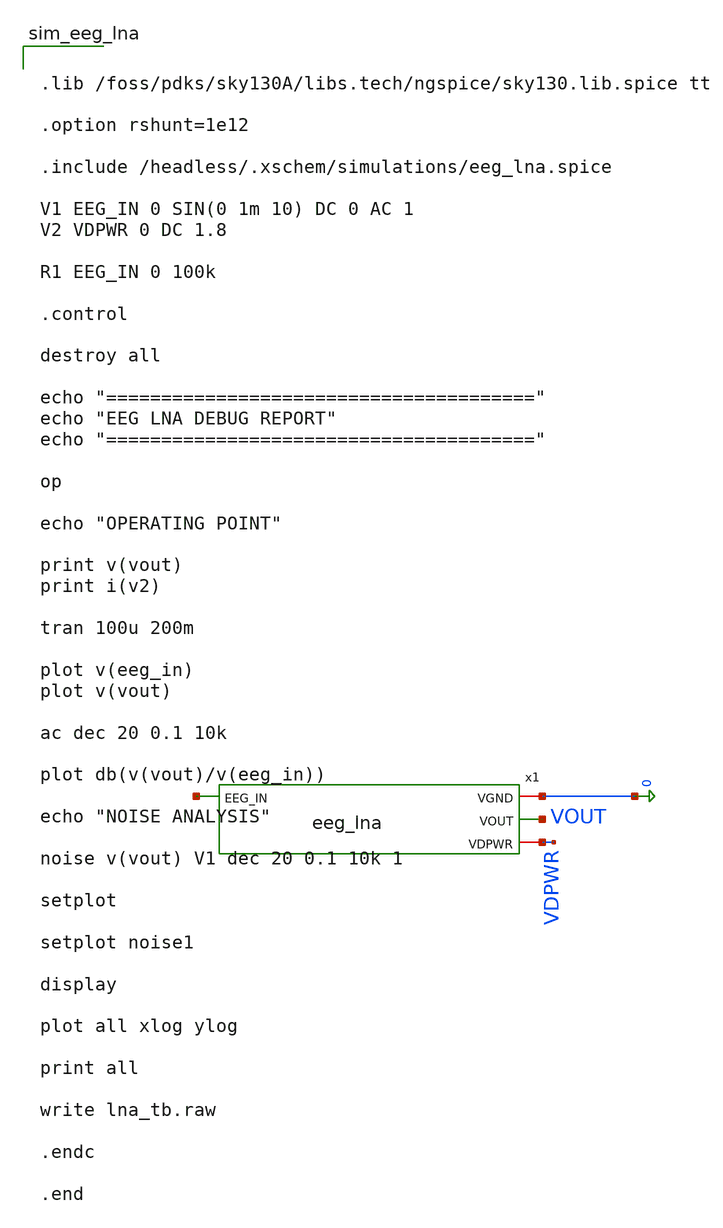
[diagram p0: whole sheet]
** sch_path: xschem/eeg_lna_tb.sch
**.subckt eeg_lna_tb
x1 net1 0 VOUT VDPWR eeg_lna
**** begin user architecture code


.lib /foss/pdks/sky130A/libs.tech/ngspice/sky130.lib.spice tt

.option rshunt=1e12

.include /headless/.xschem/simulations/eeg_lna.spice

V1 EEG_IN 0 SIN(0 1m 10) DC 0 AC 1
V2 VDPWR 0 DC 1.8

R1 EEG_IN 0 100k

.control

destroy all

echo "======================================="
echo "EEG LNA DEBUG REPORT"
echo "======================================="

op

echo "OPERATING POINT"

print v(vout)
print i(v2)

tran 100u 200m

plot v(eeg_in)
plot v(vout)

ac dec 20 0.1 10k

plot db(v(vout)/v(eeg_in))

echo "NOISE ANALYSIS"

noise v(vout) V1 dec 20 0.1 10k 1

setplot

setplot noise1

display

plot all xlog ylog

print all

write lna_tb.raw

.endc

.end


**** end user architecture code
**.ends

* expanding   symbol:  eeg_lna.sym # of pins=4
** sym_path: xschem/eeg_lna.sym
** sch_path: xschem/eeg_lna.sch
.subckt eeg_lna EEG_IN VGND VOUT VDPWR
*.iopin VGND
*.ipin EEG_IN
*.iopin VDPWR
*.opin VOUT
XM1 MIRROR_BIAS_N MIRROR_BIAS_N VGND VGND sky130_fd_pr__nfet_01v8 L=1.0 W=40 nf=1 ad='int((1 + 1)/2) * 40 / 1 * 0.29'
+ as='int((1 + 2)/2) * 40 / 1 * 0.29' pd='2*int((1 + 1)/2) * (40 / 1 + 0.29)' ps='2*int((1 + 2)/2) * (40 / 1 + 0.29)'
+ nrd='0.29 / 40 ' nrs='0.29 / 40 ' sa=0 sb=0 sd=0 mult=1 m=1
XM2 VOUT MIRROR_BIAS_N VGND VGND sky130_fd_pr__nfet_01v8 L=1.0 W=40 nf=1 ad='int((1 + 1)/2) * 40 / 1 * 0.29'
+ as='int((1 + 2)/2) * 40 / 1 * 0.29' pd='2*int((1 + 1)/2) * (40 / 1 + 0.29)' ps='2*int((1 + 2)/2) * (40 / 1 + 0.29)'
+ nrd='0.29 / 40 ' nrs='0.29 / 40 ' sa=0 sb=0 sd=0 mult=1 m=1
XM3 MIRROR_BIAS_N VIN_P TAIL_P VDPWR sky130_fd_pr__pfet_01v8 L=1.0 W=60 nf=1 ad='int((1 + 1)/2) * 60 / 1 * 0.29'
+ as='int((1 + 2)/2) * 60 / 1 * 0.29' pd='2*int((1 + 1)/2) * (60 / 1 + 0.29)' ps='2*int((1 + 2)/2) * (60 / 1 + 0.29)'
+ nrd='0.29 / 60 ' nrs='0.29 / 60 ' sa=0 sb=0 sd=0 mult=1 m=1
XM4 VOUT VIN_N TAIL_P VDPWR sky130_fd_pr__pfet_01v8 L=1.0 W=60 nf=1 ad='int((1 + 1)/2) * 60 / 1 * 0.29'
+ as='int((1 + 2)/2) * 60 / 1 * 0.29' pd='2*int((1 + 1)/2) * (60 / 1 + 0.29)' ps='2*int((1 + 2)/2) * (60 / 1 + 0.29)'
+ nrd='0.29 / 60 ' nrs='0.29 / 60 ' sa=0 sb=0 sd=0 mult=1 m=1
XM5 TAIL_P BIAS_P VDPWR VDPWR sky130_fd_pr__pfet_01v8 L=1.0 W=15 nf=1 ad='int((1 + 1)/2) * 15 / 1 * 0.29'
+ as='int((1 + 2)/2) * 15 / 1 * 0.29' pd='2*int((1 + 1)/2) * (15 / 1 + 0.29)' ps='2*int((1 + 2)/2) * (15 / 1 + 0.29)'
+ nrd='0.29 / 15 ' nrs='0.29 / 15 ' sa=0 sb=0 sd=0 mult=1 m=1
XM6 BIAS_P BIAS_P VDPWR VDPWR sky130_fd_pr__pfet_01v8 L=1.0 W=10 nf=1 ad='int((1 + 1)/2) * 10 / 1 * 0.29'
+ as='int((1 + 2)/2) * 10 / 1 * 0.29' pd='2*int((1 + 1)/2) * (10 / 1 + 0.29)' ps='2*int((1 + 2)/2) * (10 / 1 + 0.29)'
+ nrd='0.29 / 10 ' nrs='0.29 / 10 ' sa=0 sb=0 sd=0 mult=1 m=1
XM7 BIAS_P BIAS_P VGND VGND sky130_fd_pr__nfet_01v8 L=1.0 W=5 nf=1 ad='int((1 + 1)/2) * 5 / 1 * 0.29'
+ as='int((1 + 2)/2) * 5 / 1 * 0.29' pd='2*int((1 + 1)/2) * (5 / 1 + 0.29)' ps='2*int((1 + 2)/2) * (5 / 1 + 0.29)'
+ nrd='0.29 / 5 ' nrs='0.29 / 5 ' sa=0 sb=0 sd=0 mult=1 m=1
XCIN VIN_P EEG_IN sky130_fd_pr__cap_mim_m3_1 W=40 L=40 MF=1 m=1
x1 VIN_N BIAS_P pseudo_res
x2 VOUT VIN_N pseudo_res
XC1 VOUT VIN_N sky130_fd_pr__cap_mim_m3_1 W=5 L=5 MF=1 m=1
.ends


* expanding   symbol:  pseudo_res.sym # of pins=2
** sym_path: xschem/pseudo_res.sym
** sch_path: xschem/pseudo_res.sch
.subckt pseudo_res B A
*.iopin A
*.iopin B
XM1_PSEUDO_RES B B A A sky130_fd_pr__pfet_01v8 L=10 W=0.42 nf=1 ad='int((1 + 1)/2) * 0.42 / 1 * 0.29'
+ as='int((1 + 2)/2) * 0.42 / 1 * 0.29' pd='2*int((1 + 1)/2) * (0.42 / 1 + 0.29)' ps='2*int((1 + 2)/2) * (0.42 / 1 + 0.29)'
+ nrd='0.29 / 0.42 ' nrs='0.29 / 0.42 ' sa=0 sb=0 sd=0 mult=1 m=1
XM2_PSEUDO_RES A A B B sky130_fd_pr__pfet_01v8 L=10 W=0.42 nf=1 ad='int((1 + 1)/2) * 0.42 / 1 * 0.29'
+ as='int((1 + 2)/2) * 0.42 / 1 * 0.29' pd='2*int((1 + 1)/2) * (0.42 / 1 + 0.29)' ps='2*int((1 + 2)/2) * (0.42 / 1 + 0.29)'
+ nrd='0.29 / 0.42 ' nrs='0.29 / 0.42 ' sa=0 sb=0 sd=0 mult=1 m=1
.ends

.end
